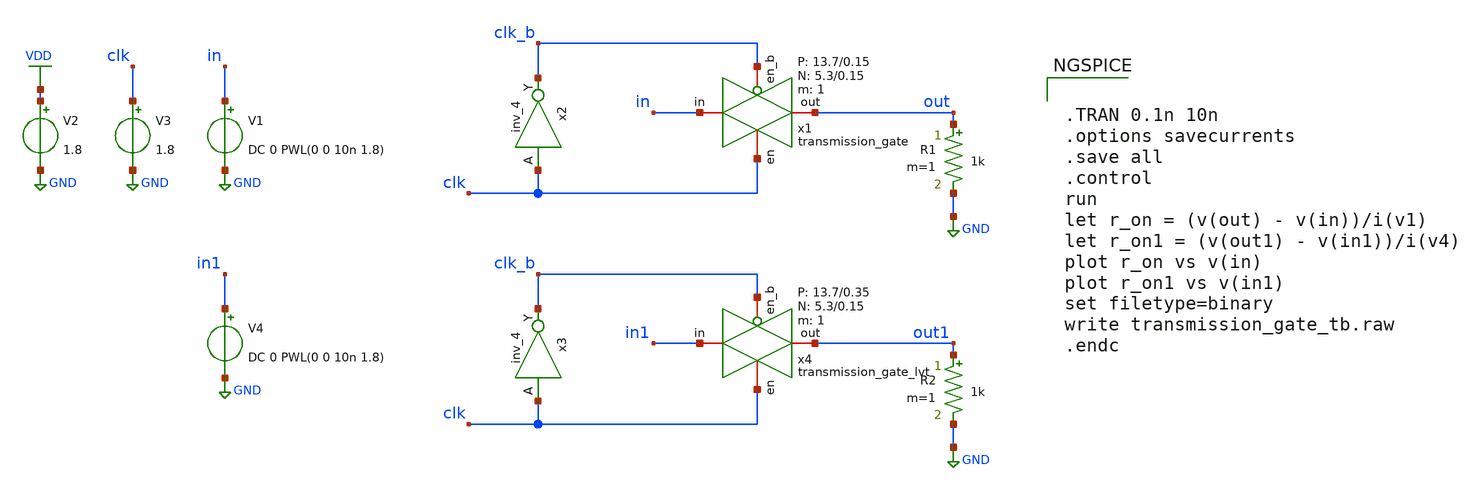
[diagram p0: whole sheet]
** sch_path: verification/schematic/transmission_gate_tb.sch
**.subckt transmission_gate_tb
x2 clk GND GND VDD VDD clk_b sky130_fd_sc_hd__inv_4
V2 VDD GND 1.8
V3 clk GND 1.8
V1 in GND DC 0 PWL(0 0 10n 1.8)
x1 in out clk clk_b VDD GND 1 5.3 0.15 13.7 0.15 transmission_gate
R1 out GND 1k m=1
V4 in1 GND DC 0 PWL(0 0 10n 1.8)
x3 clk GND GND VDD VDD clk_b sky130_fd_sc_hd__inv_4
R2 out1 GND 1k m=1
x4 in1 out1 clk clk_b VDD GND 1 5.3 0.15 13.7 0.35 transmission_gate_lvt
**** begin user architecture code


.TRAN 0.1n 10n
.options savecurrents
.save all
.control
run
let r_on = (v(out) - v(in))/i(v1)
let r_on1 = (v(out1) - v(in1))/i(v4)
plot r_on vs v(in)
plot r_on1 vs v(in1)
set filetype=binary
write transmission_gate_tb.raw
.endc



** opencircuitdesign pdks install
.lib /farmshare/home/classes/ee/372/PDKs/open_pdks_1.0.310/sky130/sky130A/libs.tech/ngspice/sky130.lib.spice tt
.inc /farmshare/home/classes/ee/372/PDKs/open_pdks_1.0.310/sky130/sky130A/libs.ref/sky130_fd_sc_hd/spice/sky130_fd_sc_hd.spice

**** end user architecture code
**.ends

* expanding   symbol:  transmission_gate.sym # of pins=4
** sym_path: design/schematic/transmission_gate.sym
** sch_path: design/schematic/transmission_gate.sch
.subckt transmission_gate in out en en_b VDD VSS N W_N L_N W_P L_P    N=1 W_N=5.3 L_N=0.15 W_P=13.7
+ L_P=0.15
*.iopin in
*.iopin out
*.ipin en
*.ipin en_b
XM1 out en in VSS sky130_fd_pr__nfet_01v8 L=L_N W=W_N nf=1 ad='int((nf+1)/2) * W/nf * 0.29' as='int((nf+2)/2) * W/nf * 0.29'
+ pd='2*int((nf+1)/2) * (W/nf + 0.29)' ps='2*int((nf+2)/2) * (W/nf + 0.29)' nrd='0.29 / W' nrs='0.29 / W'
+ sa=0 sb=0 sd=0 mult=N m=N
XM2 out en_b in VDD sky130_fd_pr__pfet_01v8 L=L_P W=W_P nf=1 ad='int((nf+1)/2) * W/nf * 0.29' as='int((nf+2)/2) * W/nf * 0.29'
+ pd='2*int((nf+1)/2) * (W/nf + 0.29)' ps='2*int((nf+2)/2) * (W/nf + 0.29)' nrd='0.29 / W' nrs='0.29 / W'
+ sa=0 sb=0 sd=0 mult=N m=N
.ends


* expanding   symbol:  transmission_gate_lvt.sym # of pins=4
** sym_path: design/schematic/transmission_gate_lvt.sym
** sch_path: design/schematic/transmission_gate_lvt.sch
.subckt transmission_gate_lvt in out en en_b VDD VSS N W_N L_N W_P L_P    N=1 W_N=5.3 L_N=0.15
+ W_P=13.7 L_P=0.35
*.iopin in
*.iopin out
*.ipin en
*.ipin en_b
XM3 out en in VSS sky130_fd_pr__nfet_01v8_lvt L=L_N W=W_N nf=1 ad='int((nf+1)/2) * W/nf * 0.29' as='int((nf+2)/2) * W/nf * 0.29'
+ pd='2*int((nf+1)/2) * (W/nf + 0.29)' ps='2*int((nf+2)/2) * (W/nf + 0.29)' nrd='0.29 / W' nrs='0.29 / W'
+ sa=0 sb=0 sd=0 mult=N m=N
XM1 out en_b in VDD sky130_fd_pr__pfet_01v8_lvt L=L_P W=W_P nf=1 ad='int((nf+1)/2) * W/nf * 0.29' as='int((nf+2)/2) * W/nf * 0.29'
+ pd='2*int((nf+1)/2) * (W/nf + 0.29)' ps='2*int((nf+2)/2) * (W/nf + 0.29)' nrd='0.29 / W' nrs='0.29 / W'
+ sa=0 sb=0 sd=0 mult=N m=N
.ends

.GLOBAL GND
.GLOBAL VDD
.end
